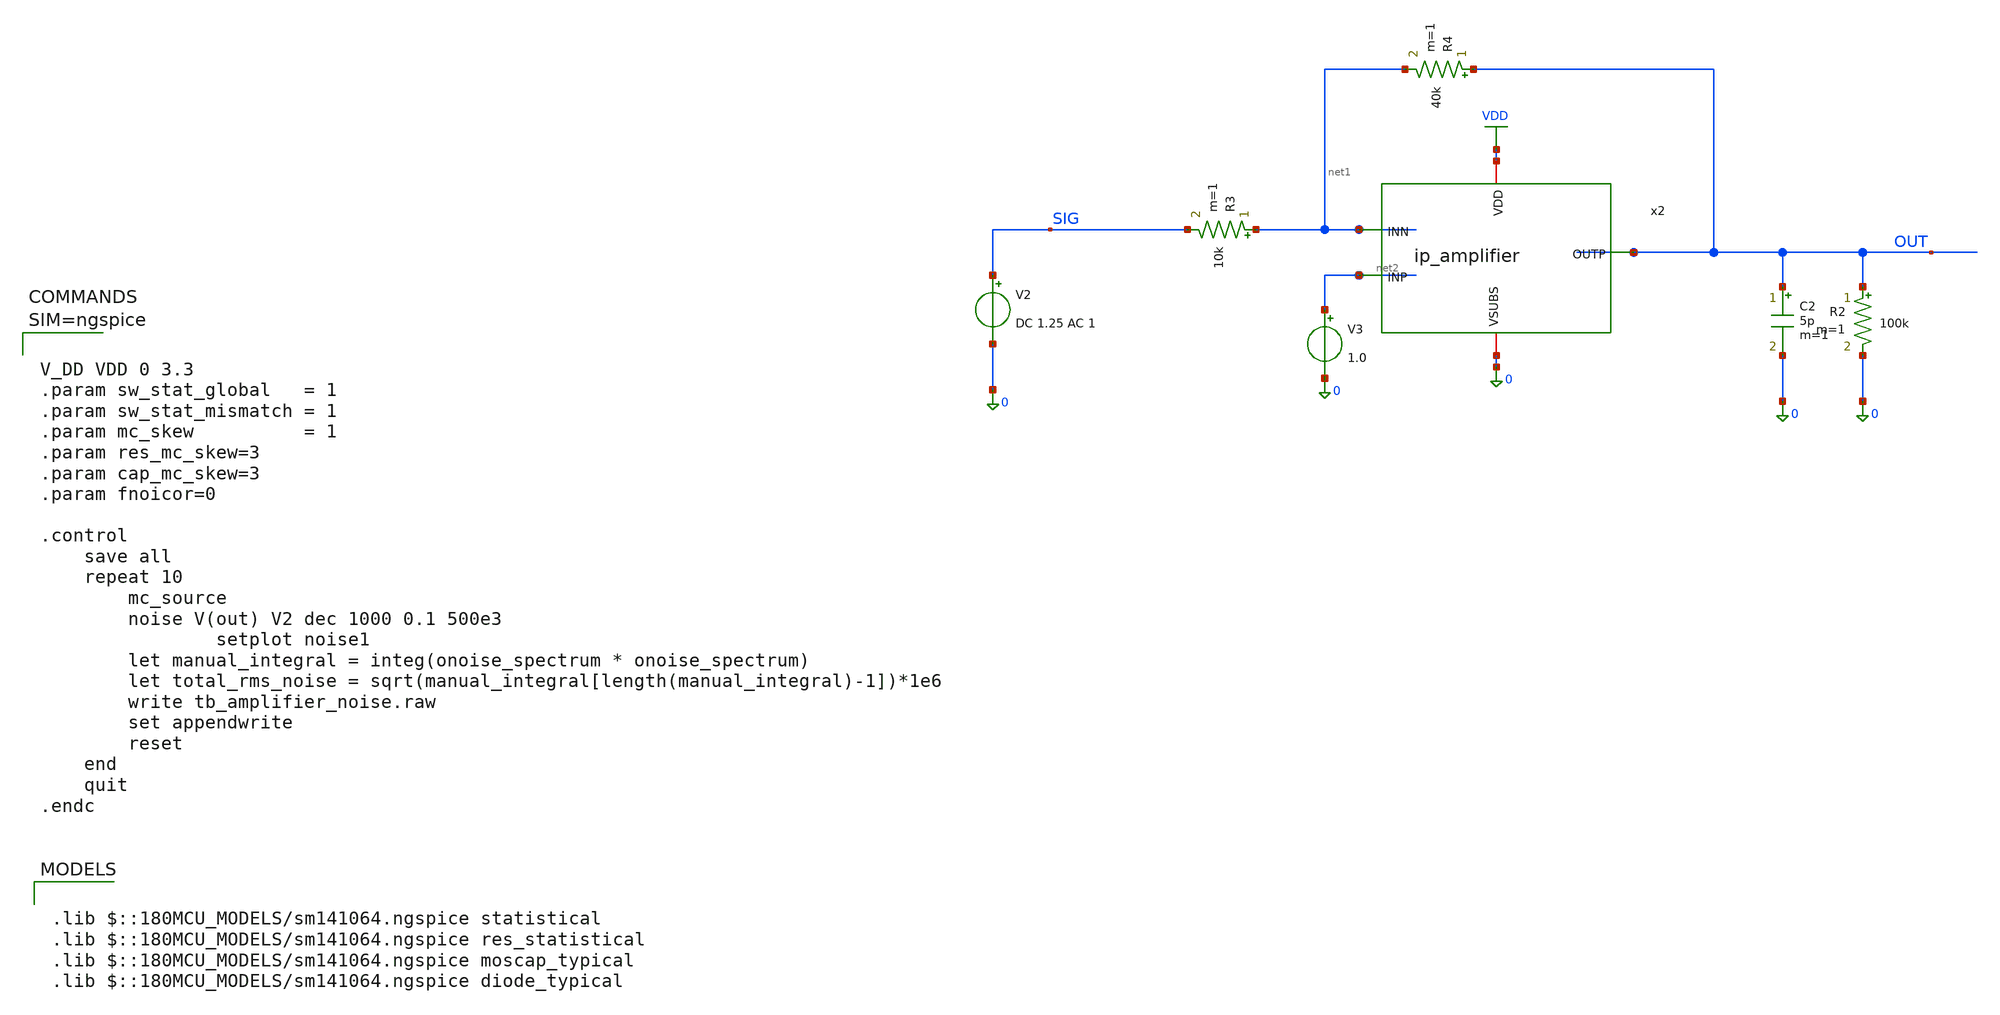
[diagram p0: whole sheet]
** sch_path: xschem/tb_amplifier_noise.sch
**.subckt tb_amplifier_noise
V2 SIG 0 DC 1.25 AC 1
x2 VDD OUT net2 net1 0 ip_amplifier
R2 OUT 0 100k m=1
C2 OUT 0 5p m=1
V3 net2 0 1.0
R3 net1 SIG 10k m=1
R4 OUT net1 40k m=1
**** begin user architecture code

.lib $::180MCU_MODELS/sm141064.ngspice statistical
.lib $::180MCU_MODELS/sm141064.ngspice res_statistical
.lib $::180MCU_MODELS/sm141064.ngspice moscap_typical
.lib $::180MCU_MODELS/sm141064.ngspice diode_typical




V_DD VDD 0 3.3
.param sw_stat_global   = 1
.param sw_stat_mismatch = 1
.param mc_skew          = 1
.param res_mc_skew=3
.param cap_mc_skew=3
.param fnoicor=0

.control
	save all
	repeat 10
		mc_source
		noise V(out) V2 dec 1000 0.1 500e3
                setplot noise1
		let manual_integral = integ(onoise_spectrum * onoise_spectrum)
		let total_rms_noise = sqrt(manual_integral[length(manual_integral)-1])*1e6
		write tb_amplifier_noise.raw
		set appendwrite
		reset
	end
	quit
.endc



**** end user architecture code
**.ends

* expanding   symbol:  ip_amplifier.sym # of pins=5
** sym_path: xschem/ip_amplifier.sym
** sch_path: xschem/ip_amplifier.sch
.subckt ip_amplifier VDD OUTP INP INN VSUBS
*.iopin VDD
*.iopin VSUBS
*.ipin INP
*.ipin INN
*.opin OUTP
XM1 net10 INP net8 VDD pfet_06v0 L=0.7u W=7.0u nf=1 ad='int((nf+1)/2) * W/nf * 0.18u' as='int((nf+2)/2) * W/nf * 0.18u'
+ pd='2*int((nf+1)/2) * (W/nf + 0.18u)' ps='2*int((nf+2)/2) * (W/nf + 0.18u)' nrd='0.18u / W' nrs='0.18u / W'
+ sa=0 sb=0 sd=0 m=2 par=2
XM2 net9 INN net8 VDD pfet_06v0 L=0.7u W=7.0u nf=1 ad='int((nf+1)/2) * W/nf * 0.18u' as='int((nf+2)/2) * W/nf * 0.18u'
+ pd='2*int((nf+1)/2) * (W/nf + 0.18u)' ps='2*int((nf+2)/2) * (W/nf + 0.18u)' nrd='0.18u / W' nrs='0.18u / W'
+ sa=0 sb=0 sd=0 m=2 par=2
XM5 net10 net1 VSUBS vsubs nfet_06v0 L=3u W=3u nf=1 ad='int((nf+1)/2) * W/nf * 0.18u' as='int((nf+2)/2) * W/nf * 0.18u'
+ pd='2*int((nf+1)/2) * (W/nf + 0.18u)' ps='2*int((nf+2)/2) * (W/nf + 0.18u)' nrd='0.18u / W' nrs='0.18u / W'
+ sa=0 sb=0 sd=0 m=1 par=1
XM6 net9 net1 VSUBS vsubs nfet_06v0 L=3u W=3u nf=1 ad='int((nf+1)/2) * W/nf * 0.18u' as='int((nf+2)/2) * W/nf * 0.18u'
+ pd='2*int((nf+1)/2) * (W/nf + 0.18u)' ps='2*int((nf+2)/2) * (W/nf + 0.18u)' nrd='0.18u / W' nrs='0.18u / W'
+ sa=0 sb=0 sd=0 m=1 par=1
XM3 net3 net1 VSUBS vsubs nfet_06v0 L=1u W=5u nf=1 ad='int((nf+1)/2) * W/nf * 0.18u' as='int((nf+2)/2) * W/nf * 0.18u'
+ pd='2*int((nf+1)/2) * (W/nf + 0.18u)' ps='2*int((nf+2)/2) * (W/nf + 0.18u)' nrd='0.18u / W' nrs='0.18u / W'
+ sa=0 sb=0 sd=0 m=5 par=5
XM4 net2 net1 VSUBS vsubs nfet_06v0 L=1u W=5u nf=1 ad='int((nf+1)/2) * W/nf * 0.18u' as='int((nf+2)/2) * W/nf * 0.18u'
+ pd='2*int((nf+1)/2) * (W/nf + 0.18u)' ps='2*int((nf+2)/2) * (W/nf + 0.18u)' nrd='0.18u / W' nrs='0.18u / W'
+ sa=0 sb=0 sd=0 m=1 par=1
XM7 net1 net1 net3 vsubs nfet_06v0 L=0.7u W=5u nf=1 ad='int((nf+1)/2) * W/nf * 0.18u' as='int((nf+2)/2) * W/nf * 0.18u'
+ pd='2*int((nf+1)/2) * (W/nf + 0.18u)' ps='2*int((nf+2)/2) * (W/nf + 0.18u)' nrd='0.18u / W' nrs='0.18u / W'
+ sa=0 sb=0 sd=0 m=7 par=7
XM8 net4 net1 net2 vsubs nfet_06v0 L=0.7u W=5u nf=1 ad='int((nf+1)/2) * W/nf * 0.18u' as='int((nf+2)/2) * W/nf * 0.18u'
+ pd='2*int((nf+1)/2) * (W/nf + 0.18u)' ps='2*int((nf+2)/2) * (W/nf + 0.18u)' nrd='0.18u / W' nrs='0.18u / W'
+ sa=0 sb=0 sd=0 m=7 par=7
XM9 net5 net7 VDD VDD pfet_06v0 L=1u W=6u nf=1 ad='int((nf+1)/2) * W/nf * 0.18u' as='int((nf+2)/2) * W/nf * 0.18u'
+ pd='2*int((nf+1)/2) * (W/nf + 0.18u)' ps='2*int((nf+2)/2) * (W/nf + 0.18u)' nrd='0.18u / W' nrs='0.18u / W'
+ sa=0 sb=0 sd=0 m=1 par=1
XM10 net6 net7 VDD VDD pfet_06v0 L=1u W=6u nf=1 ad='int((nf+1)/2) * W/nf * 0.18u' as='int((nf+2)/2) * W/nf * 0.18u'
+ pd='2*int((nf+1)/2) * (W/nf + 0.18u)' ps='2*int((nf+2)/2) * (W/nf + 0.18u)' nrd='0.18u / W' nrs='0.18u / W'
+ sa=0 sb=0 sd=0 m=1 par=1
XM11 net7 net7 net5 VDD pfet_06v0 L=0.7u W=7u nf=1 ad='int((nf+1)/2) * W/nf * 0.18u' as='int((nf+2)/2) * W/nf * 0.18u'
+ pd='2*int((nf+1)/2) * (W/nf + 0.18u)' ps='2*int((nf+2)/2) * (W/nf + 0.18u)' nrd='0.18u / W' nrs='0.18u / W'
+ sa=0 sb=0 sd=0 m=5 par=5
XM12 net8 net7 net6 VDD pfet_06v0 L=0.7u W=7u nf=1 ad='int((nf+1)/2) * W/nf * 0.18u' as='int((nf+2)/2) * W/nf * 0.18u'
+ pd='2*int((nf+1)/2) * (W/nf + 0.18u)' ps='2*int((nf+2)/2) * (W/nf + 0.18u)' nrd='0.18u / W' nrs='0.18u / W'
+ sa=0 sb=0 sd=0 m=5 par=5
XM13 net11 net1 net9 vsubs nfet_06v0 L=0.7u W=7u nf=1 ad='int((nf+1)/2) * W/nf * 0.18u' as='int((nf+2)/2) * W/nf * 0.18u'
+ pd='2*int((nf+1)/2) * (W/nf + 0.18u)' ps='2*int((nf+2)/2) * (W/nf + 0.18u)' nrd='0.18u / W' nrs='0.18u / W'
+ sa=0 sb=0 sd=0 m=5 par=5
XM14 net12 net1 net10 vsubs nfet_06v0 L=0.7u W=7u nf=1 ad='int((nf+1)/2) * W/nf * 0.18u' as='int((nf+2)/2) * W/nf * 0.18u'
+ pd='2*int((nf+1)/2) * (W/nf + 0.18u)' ps='2*int((nf+2)/2) * (W/nf + 0.18u)' nrd='0.18u / W' nrs='0.18u / W'
+ sa=0 sb=0 sd=0 m=5 par=5
XM15 net11 net11 VDD VDD pfet_06v0 L=0.7u W=7u nf=1 ad='int((nf+1)/2) * W/nf * 0.18u' as='int((nf+2)/2) * W/nf * 0.18u'
+ pd='2*int((nf+1)/2) * (W/nf + 0.18u)' ps='2*int((nf+2)/2) * (W/nf + 0.18u)' nrd='0.18u / W' nrs='0.18u / W'
+ sa=0 sb=0 sd=0 m=1 par=1
XM16 net12 net11 VDD VDD pfet_06v0 L=0.7u W=7u nf=1 ad='int((nf+1)/2) * W/nf * 0.18u' as='int((nf+2)/2) * W/nf * 0.18u'
+ pd='2*int((nf+1)/2) * (W/nf + 0.18u)' ps='2*int((nf+2)/2) * (W/nf + 0.18u)' nrd='0.18u / W' nrs='0.18u / W'
+ sa=0 sb=0 sd=0 m=1 par=1
XM17 OUTP net12 VDD VDD pfet_06v0 L=0.5u W=5u nf=1 ad='int((nf+1)/2) * W/nf * 0.18u' as='int((nf+2)/2) * W/nf * 0.18u'
+ pd='2*int((nf+1)/2) * (W/nf + 0.18u)' ps='2*int((nf+2)/2) * (W/nf + 0.18u)' nrd='0.18u / W' nrs='0.18u / W'
+ sa=0 sb=0 sd=0 m=6 par=6
XM18 OUTP net10 VSUBS vsubs nfet_06v0 L=0.7u W=5u nf=1 ad='int((nf+1)/2) * W/nf * 0.18u' as='int((nf+2)/2) * W/nf * 0.18u'
+ pd='2*int((nf+1)/2) * (W/nf + 0.18u)' ps='2*int((nf+2)/2) * (W/nf + 0.18u)' nrd='0.18u / W' nrs='0.18u / W'
+ sa=0 sb=0 sd=0 m=2 par=2
XR3 net1 net15 vsubs ppolyf_u_1k_6p0 r_width=1e-6 r_length=6e-6 m=1
XR6 net15 net14 vsubs ppolyf_u_1k_6p0 r_width=1e-6 r_length=6e-6 m=1
XR7 net14 net13 vsubs ppolyf_u_1k_6p0 r_width=1e-6 r_length=6e-6 m=1
XR8 net13 net16 vsubs ppolyf_u_1k_6p0 r_width=1e-6 r_length=4e-6 m=1
Vmeas VDD net16 0
Vmeas1 net7 net4 0
XC1 net12 OUTP cap_nmos_03v3 c_width=15e-6 c_length=15e-6 m=1
.ends

.GLOBAL VDD
.end
